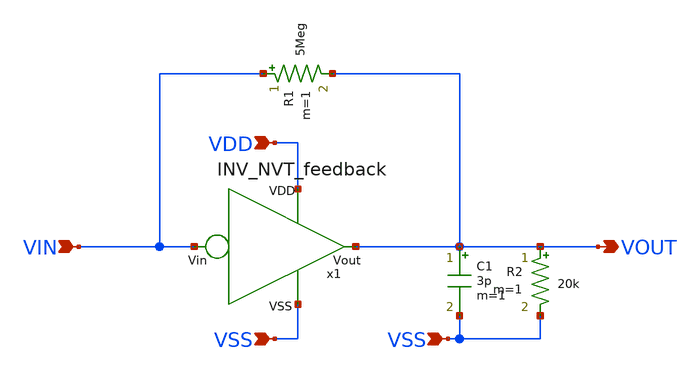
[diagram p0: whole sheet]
** sch_path: design/THESIS_EXP_RO_INVERTER_SKY130A/TB_large_scale.sch
**.subckt TB_large_scale VDD VSS VSS VIN VOUT
*.ipin VDD
*.ipin VSS
*.ipin VSS
*.ipin VIN
*.opin VOUT
R1 VIN VOUT 5Meg m=1
R2 VOUT VSS 20k m=1
C1 VOUT VSS 3p m=1
x1 VDD VSS VOUT VIN INV_NVT_feedback
**.ends

* expanding   symbol:  THESIS_EXP_RO_INVERTER_SKY130A/INV_NVT_feedback.sym # of pins=4
** sym_path: design/THESIS_EXP_RO_INVERTER_SKY130A/INV_NVT_feedback.sym
** sch_path: design/THESIS_EXP_RO_INVERTER_SKY130A/INV_NVT_feedback.sch
.subckt INV_NVT_feedback VDD VSS Vout Vin
*.ipin VSS
*.ipin Vin
*.opin Vout
*.ipin VDD
XM1 Vout Vin net4 net4 sky130_fd_pr__pfet_01v8_lvt L=0.35 W=7 nf=1 ad='int((nf+1)/2) * W/nf * 0.29' as='int((nf+2)/2) * W/nf * 0.29'
+ pd='2*int((nf+1)/2) * (W/nf + 0.29)' ps='2*int((nf+2)/2) * (W/nf + 0.29)' nrd='0.29 / W' nrs='0.29 / W'
+ sa=0 sb=0 sd=0 mult=m_alpha m=m_alpha
XM2 net1 Vin vn VSS sky130_fd_pr__nfet_03v3_nvt L=0.6 W=1 nf=1 ad='int((nf+1)/2) * W/nf * 0.29' as='int((nf+2)/2) * W/nf * 0.29'
+ pd='2*int((nf+1)/2) * (W/nf + 0.29)' ps='2*int((nf+2)/2) * (W/nf + 0.29)' nrd='0.29 / W' nrs='0.29 / W'
+ sa=0 sb=0 sd=0 mult=m_beta m=m_beta
XM3 net2 Vin VSS VSS sky130_fd_pr__nfet_03v3_nvt L=0.6 W=1 nf=1 ad='int((nf+1)/2) * W/nf * 0.29' as='int((nf+2)/2) * W/nf * 0.29'
+ pd='2*int((nf+1)/2) * (W/nf + 0.29)' ps='2*int((nf+2)/2) * (W/nf + 0.29)' nrd='0.29 / W' nrs='0.29 / W'
+ sa=0 sb=0 sd=0 mult=m_I0 m=m_I0
XM4 VDD Vout net3 VSS sky130_fd_pr__nfet_03v3_nvt L=0.6 W=1 nf=1 ad='int((nf+1)/2) * W/nf * 0.29' as='int((nf+2)/2) * W/nf * 0.29'
+ pd='2*int((nf+1)/2) * (W/nf + 0.29)' ps='2*int((nf+2)/2) * (W/nf + 0.29)' nrd='0.29 / W' nrs='0.29 / W'
+ sa=0 sb=0 sd=0 mult=m_gamma m=m_gamma
V1 VDD net4 0
.save i(v1)
V2 Vout net1 0
.save i(v2)
V3 vn net2 0
.save i(v3)
V4 net3 vn 0
.save i(v4)
.ends

.end
